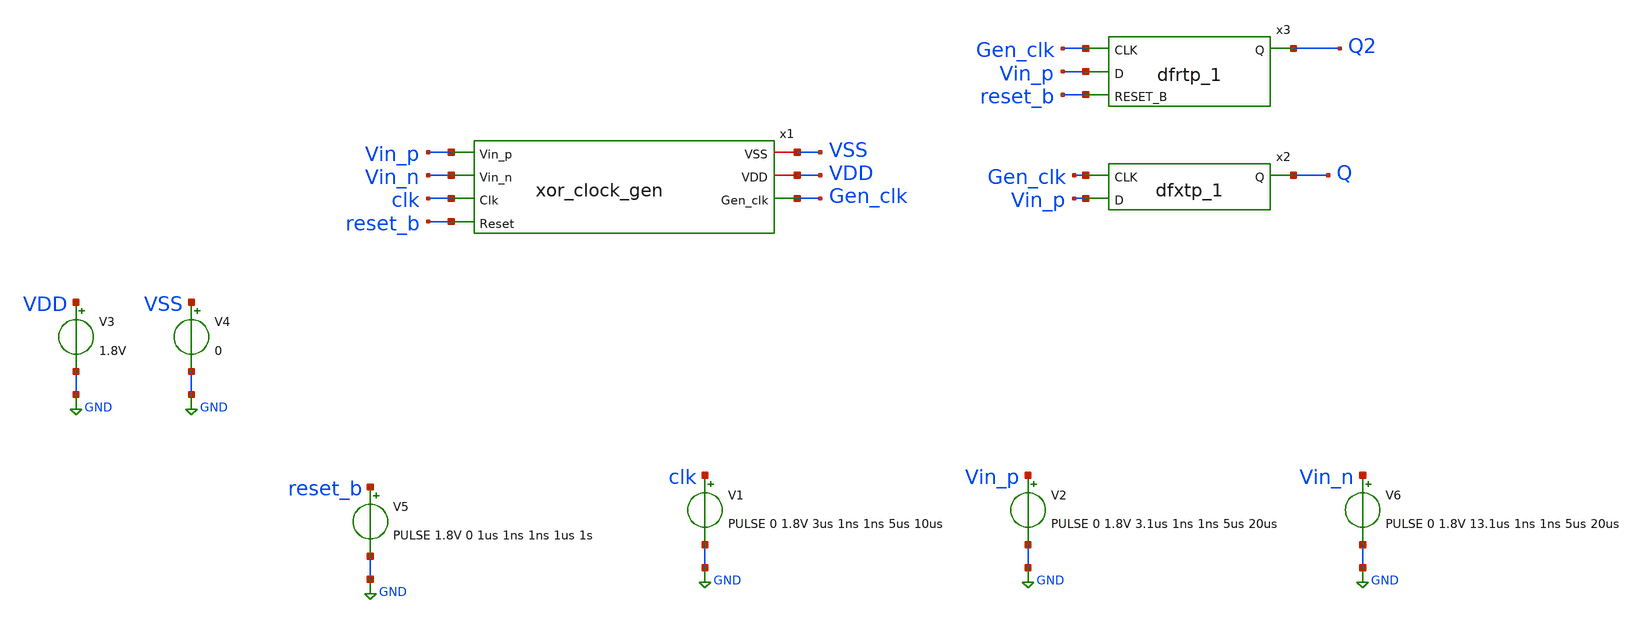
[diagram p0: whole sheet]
** sch_path: xschem/tests/xor_clock_gen/xor_clock_gen_timing_test.sch
**.subckt xor_clock_gen_timing_test
V3 VDD GND 1.8V
V4 VSS GND 0
x1 VSS Vin_p VDD Vin_n Gen_clk clk reset_b xor_clock_gen
V5 reset_b GND PULSE 1.8V 0 1us 1ns 1ns 1us 1s
V1 clk GND PULSE 0 1.8V 3us 1ns 1ns 5us 10us
V2 Vin_p GND PULSE 0 1.8V 3.1us 1ns 1ns 5us 20us
V6 Vin_n GND PULSE 0 1.8V 13.1us 1ns 1ns 5us 20us
x2 Gen_clk Vin_p VSS VSS VDD VDD Q sky130_fd_sc_hd__dfxtp_1
x3 Gen_clk Vin_p reset_b VSS VSS VDD VDD Q2 sky130_fd_sc_hd__dfrtp_1
**** begin user architecture code
 .lib $::SKYWATER_MODELS/sky130.lib.spice tt
.include $::SKYWATER_STDCELLS/sky130_fd_sc_hd.spice


.options acct list
.temp 25
*vvcc VDD 0 dc 1.8
*vvss VSS 0 0
.control
tran 0.01u 11u
*plot RST_PLS clk+2 Pulse+4
plot Vin_p-Vin_n clk reset_b-2 Gen_clk Q+2 Q2+4
write xor_clock_gen_timing_test.raw
.endc


**** end user architecture code
**.ends

* expanding   symbol:  src/xor_clock_gen/xor_clock_gen.sym # of pins=7
** sym_path: xschem/src/xor_clock_gen/xor_clock_gen.sym
** sch_path: xschem/src/xor_clock_gen/xor_clock_gen.sch
.subckt xor_clock_gen VSS Vin_p VDD Vin_n Gen_clk Clk Reset
*.ipin Vin_p
*.iopin VSS
*.opin Gen_clk
*.iopin VDD
*.ipin Vin_n
*.ipin Clk
*.ipin Reset
x1 Vin_p Vin_n VSS VSS VDD VDD net1 sky130_fd_sc_hd__xor2_1
x3 net1 VSS VSS VDD VDD net6 sky130_fd_sc_hd__inv_1
x6 net1 net2 Reset VSS VSS VDD VDD net5 net2 sky130_fd_sc_hd__dfrbp_1
x2 net6 net3 Reset VSS VSS VDD VDD net4 net3 sky130_fd_sc_hd__dfrbp_1
x4 net5 net4 VSS VSS VDD VDD Gen_clk sky130_fd_sc_hd__xor2_1
.ends

.GLOBAL GND
.end
